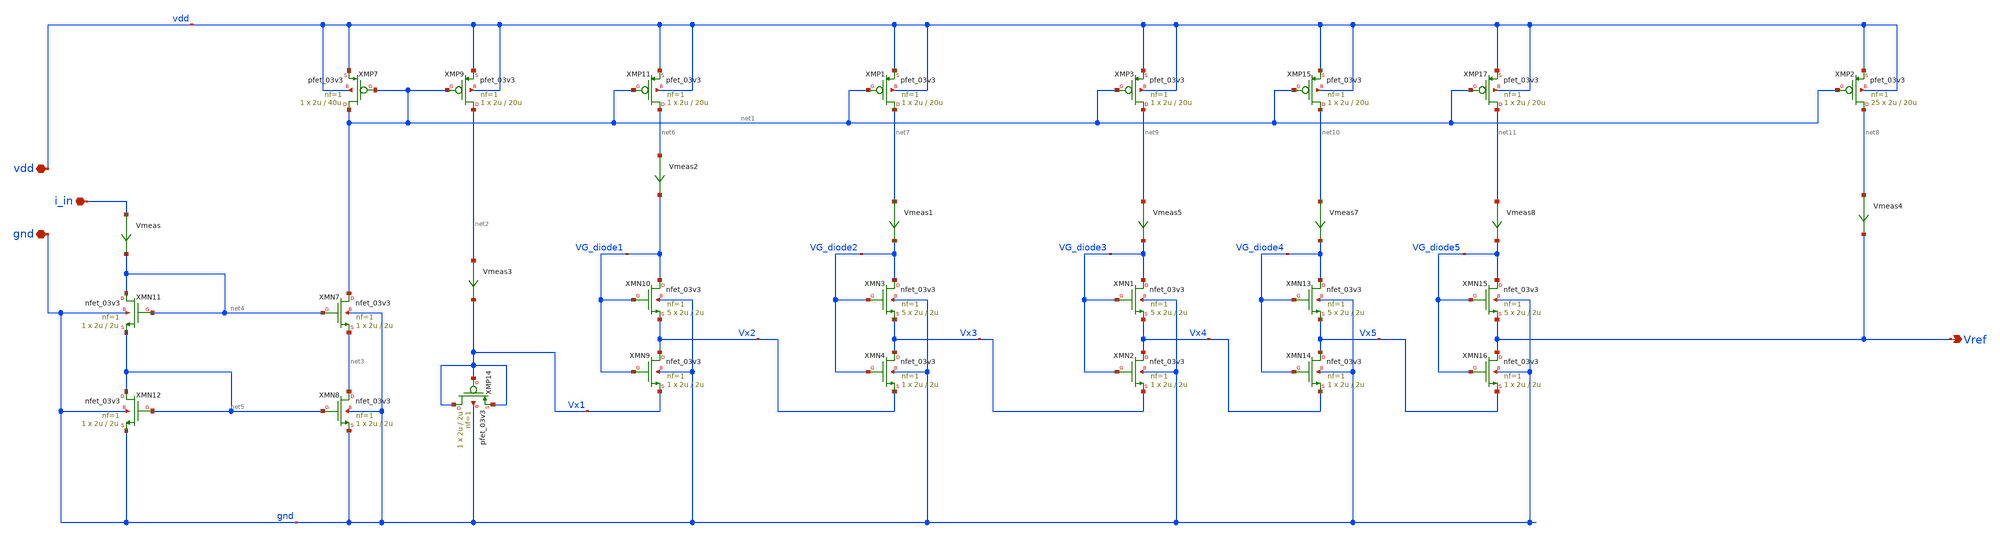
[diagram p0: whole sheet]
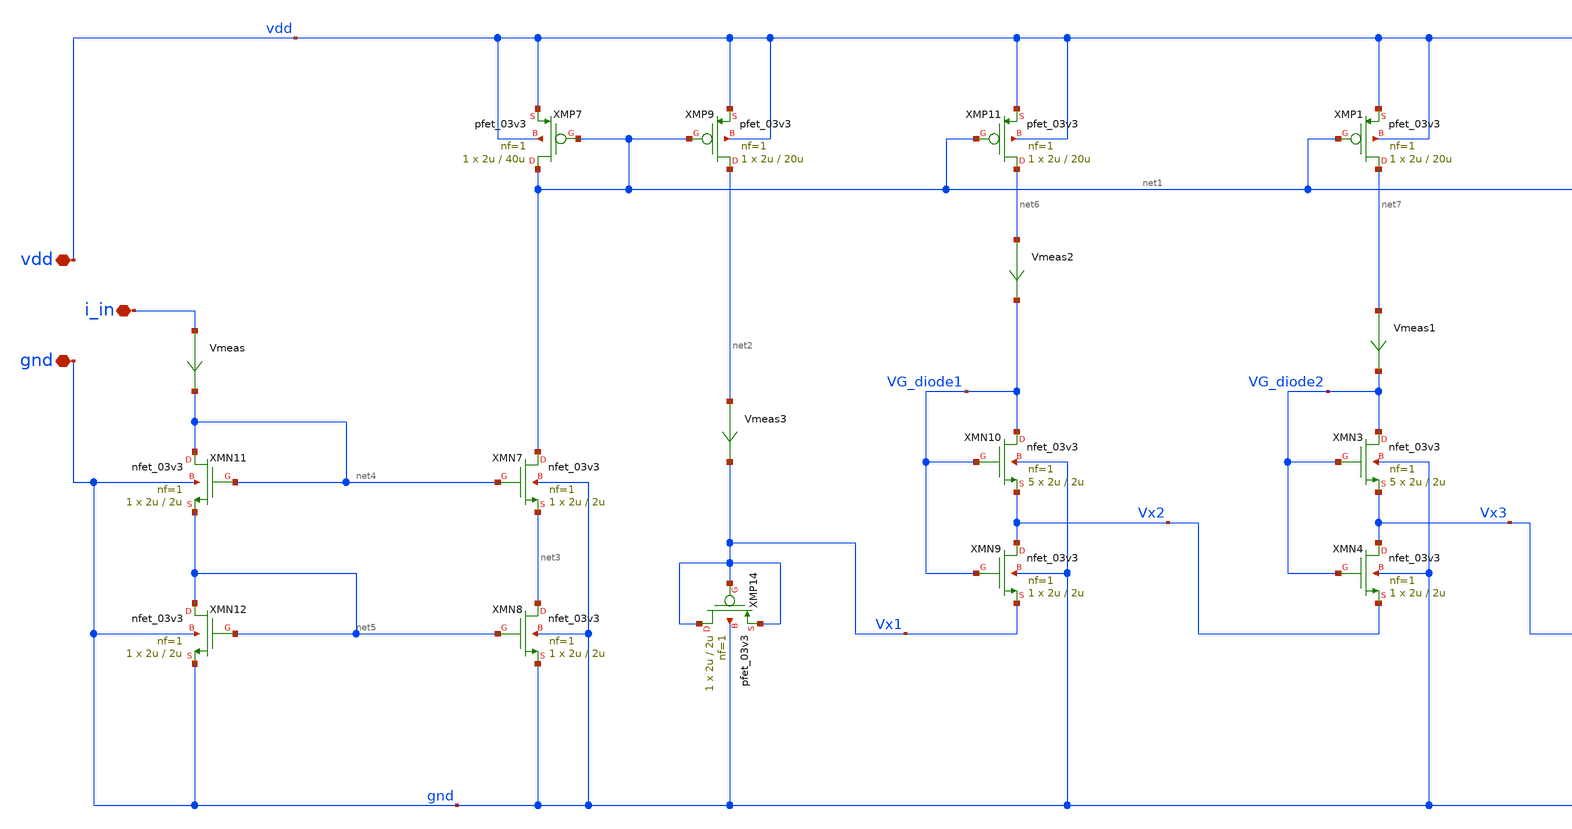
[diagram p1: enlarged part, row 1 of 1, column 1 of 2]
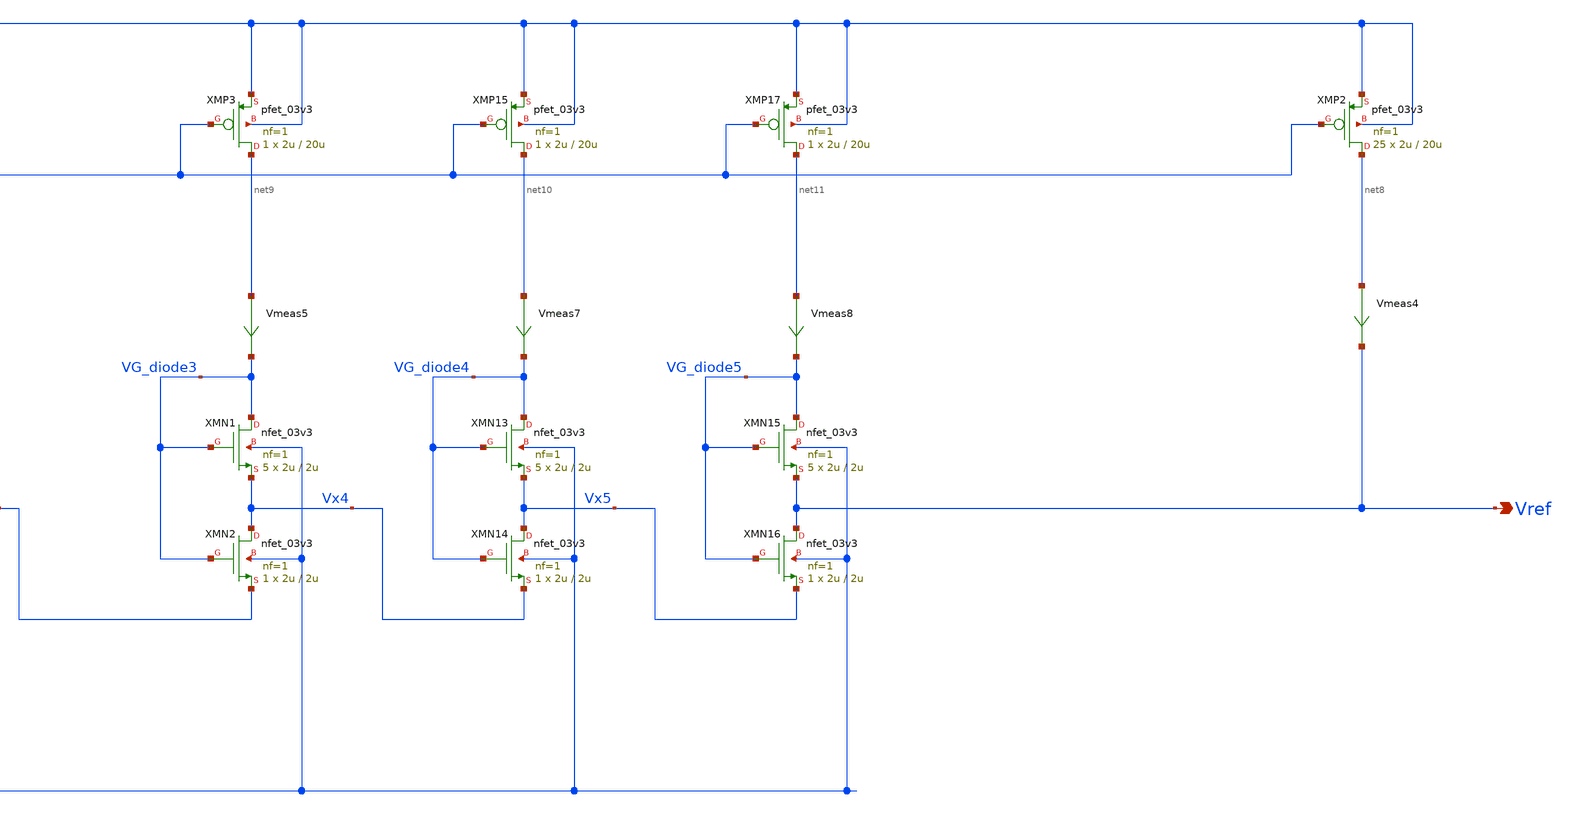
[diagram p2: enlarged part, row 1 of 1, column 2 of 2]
** sch_path: Voltage_Reference/symbols_vr/Voltage_Reference.sch
**.subckt Voltage_Reference i_in vdd gnd Vref
*.iopin i_in
*.iopin vdd
*.iopin gnd
*.opin Vref
XMP7 net1 net1 vdd vdd pfet_03v3 L=40u W=2u nf=1 ad='int((nf+1)/2) * W/nf * 0.18u' as='int((nf+2)/2) * W/nf * 0.18u'
+ pd='2*int((nf+1)/2) * (W/nf + 0.18u)' ps='2*int((nf+2)/2) * (W/nf + 0.18u)' nrd='0.18u / W' nrs='0.18u / W'
+ sa=0 sb=0 sd=0 m=1
XMP9 net2 net1 vdd vdd pfet_03v3 L=20u W=2u nf=1 ad='int((nf+1)/2) * W/nf * 0.18u' as='int((nf+2)/2) * W/nf * 0.18u'
+ pd='2*int((nf+1)/2) * (W/nf + 0.18u)' ps='2*int((nf+2)/2) * (W/nf + 0.18u)' nrd='0.18u / W' nrs='0.18u / W'
+ sa=0 sb=0 sd=0 m=1
XMN7 net1 net4 net3 gnd nfet_03v3 L=2u W=2u nf=1 ad='int((nf+1)/2) * W/nf * 0.18u' as='int((nf+2)/2) * W/nf * 0.18u'
+ pd='2*int((nf+1)/2) * (W/nf + 0.18u)' ps='2*int((nf+2)/2) * (W/nf + 0.18u)' nrd='0.18u / W' nrs='0.18u / W'
+ sa=0 sb=0 sd=0 m=1
XMN8 net3 net5 gnd gnd nfet_03v3 L=2u W=2u nf=1 ad='int((nf+1)/2) * W/nf * 0.18u' as='int((nf+2)/2) * W/nf * 0.18u'
+ pd='2*int((nf+1)/2) * (W/nf + 0.18u)' ps='2*int((nf+2)/2) * (W/nf + 0.18u)' nrd='0.18u / W' nrs='0.18u / W'
+ sa=0 sb=0 sd=0 m=1
XMP14 Vx1 Vx1 Vx1 gnd pfet_03v3 L=2u W=2u nf=1 ad='int((nf+1)/2) * W/nf * 0.18u' as='int((nf+2)/2) * W/nf * 0.18u'
+ pd='2*int((nf+1)/2) * (W/nf + 0.18u)' ps='2*int((nf+2)/2) * (W/nf + 0.18u)' nrd='0.18u / W' nrs='0.18u / W'
+ sa=0 sb=0 sd=0 m=1
XMP11 net6 net1 vdd vdd pfet_03v3 L=20u W=2u nf=1 ad='int((nf+1)/2) * W/nf * 0.18u' as='int((nf+2)/2) * W/nf * 0.18u'
+ pd='2*int((nf+1)/2) * (W/nf + 0.18u)' ps='2*int((nf+2)/2) * (W/nf + 0.18u)' nrd='0.18u / W' nrs='0.18u / W'
+ sa=0 sb=0 sd=0 m=1
XMN10 VG_diode1 VG_diode1 Vx2 gnd nfet_03v3 L=2u W=2u nf=1 ad='int((nf+1)/2) * W/nf * 0.18u' as='int((nf+2)/2) * W/nf * 0.18u'
+ pd='2*int((nf+1)/2) * (W/nf + 0.18u)' ps='2*int((nf+2)/2) * (W/nf + 0.18u)' nrd='0.18u / W' nrs='0.18u / W'
+ sa=0 sb=0 sd=0 m=5
XMN9 Vx2 VG_diode1 Vx1 gnd nfet_03v3 L=2u W=2u nf=1 ad='int((nf+1)/2) * W/nf * 0.18u' as='int((nf+2)/2) * W/nf * 0.18u'
+ pd='2*int((nf+1)/2) * (W/nf + 0.18u)' ps='2*int((nf+2)/2) * (W/nf + 0.18u)' nrd='0.18u / W' nrs='0.18u / W'
+ sa=0 sb=0 sd=0 m=1
XMN11 net4 net4 net5 gnd nfet_03v3 L=2u W=2u nf=1 ad='int((nf+1)/2) * W/nf * 0.18u' as='int((nf+2)/2) * W/nf * 0.18u'
+ pd='2*int((nf+1)/2) * (W/nf + 0.18u)' ps='2*int((nf+2)/2) * (W/nf + 0.18u)' nrd='0.18u / W' nrs='0.18u / W'
+ sa=0 sb=0 sd=0 m=1
XMN12 net5 net5 gnd gnd nfet_03v3 L=2u W=2u nf=1 ad='int((nf+1)/2) * W/nf * 0.18u' as='int((nf+2)/2) * W/nf * 0.18u'
+ pd='2*int((nf+1)/2) * (W/nf + 0.18u)' ps='2*int((nf+2)/2) * (W/nf + 0.18u)' nrd='0.18u / W' nrs='0.18u / W'
+ sa=0 sb=0 sd=0 m=1
Vmeas i_in net4 0
.save i(vmeas)
Vmeas3 net2 Vx1 0
.save i(vmeas3)
XMN3 VG_diode2 VG_diode2 Vx3 gnd nfet_03v3 L=2u W=2u nf=1 ad='int((nf+1)/2) * W/nf * 0.18u' as='int((nf+2)/2) * W/nf * 0.18u'
+ pd='2*int((nf+1)/2) * (W/nf + 0.18u)' ps='2*int((nf+2)/2) * (W/nf + 0.18u)' nrd='0.18u / W' nrs='0.18u / W'
+ sa=0 sb=0 sd=0 m=5
XMN4 Vx3 VG_diode2 Vx2 gnd nfet_03v3 L=2u W=2u nf=1 ad='int((nf+1)/2) * W/nf * 0.18u' as='int((nf+2)/2) * W/nf * 0.18u'
+ pd='2*int((nf+1)/2) * (W/nf + 0.18u)' ps='2*int((nf+2)/2) * (W/nf + 0.18u)' nrd='0.18u / W' nrs='0.18u / W'
+ sa=0 sb=0 sd=0 m=1
Vmeas1 net7 VG_diode2 0
.save i(vmeas1)
Vmeas2 net6 VG_diode1 0
.save i(vmeas2)
XMP1 net7 net1 vdd vdd pfet_03v3 L=20u W=2u nf=1 ad='int((nf+1)/2) * W/nf * 0.18u' as='int((nf+2)/2) * W/nf * 0.18u'
+ pd='2*int((nf+1)/2) * (W/nf + 0.18u)' ps='2*int((nf+2)/2) * (W/nf + 0.18u)' nrd='0.18u / W' nrs='0.18u / W'
+ sa=0 sb=0 sd=0 m=1
XMP2 net8 net1 vdd vdd pfet_03v3 L=20u W=2u nf=1 ad='int((nf+1)/2) * W/nf * 0.18u' as='int((nf+2)/2) * W/nf * 0.18u'
+ pd='2*int((nf+1)/2) * (W/nf + 0.18u)' ps='2*int((nf+2)/2) * (W/nf + 0.18u)' nrd='0.18u / W' nrs='0.18u / W'
+ sa=0 sb=0 sd=0 m=25
Vmeas4 net8 Vref 0
.save i(vmeas4)
XMN1 VG_diode3 VG_diode3 Vx4 gnd nfet_03v3 L=2u W=2u nf=1 ad='int((nf+1)/2) * W/nf * 0.18u' as='int((nf+2)/2) * W/nf * 0.18u'
+ pd='2*int((nf+1)/2) * (W/nf + 0.18u)' ps='2*int((nf+2)/2) * (W/nf + 0.18u)' nrd='0.18u / W' nrs='0.18u / W'
+ sa=0 sb=0 sd=0 m=5
XMN2 Vx4 VG_diode3 Vx3 gnd nfet_03v3 L=2u W=2u nf=1 ad='int((nf+1)/2) * W/nf * 0.18u' as='int((nf+2)/2) * W/nf * 0.18u'
+ pd='2*int((nf+1)/2) * (W/nf + 0.18u)' ps='2*int((nf+2)/2) * (W/nf + 0.18u)' nrd='0.18u / W' nrs='0.18u / W'
+ sa=0 sb=0 sd=0 m=1
Vmeas5 net9 VG_diode3 0
.save i(vmeas5)
XMP3 net9 net1 vdd vdd pfet_03v3 L=20u W=2u nf=1 ad='int((nf+1)/2) * W/nf * 0.18u' as='int((nf+2)/2) * W/nf * 0.18u'
+ pd='2*int((nf+1)/2) * (W/nf + 0.18u)' ps='2*int((nf+2)/2) * (W/nf + 0.18u)' nrd='0.18u / W' nrs='0.18u / W'
+ sa=0 sb=0 sd=0 m=1
XMN13 VG_diode4 VG_diode4 Vx5 gnd nfet_03v3 L=2u W=2u nf=1 ad='int((nf+1)/2) * W/nf * 0.18u' as='int((nf+2)/2) * W/nf * 0.18u'
+ pd='2*int((nf+1)/2) * (W/nf + 0.18u)' ps='2*int((nf+2)/2) * (W/nf + 0.18u)' nrd='0.18u / W' nrs='0.18u / W'
+ sa=0 sb=0 sd=0 m=5
XMN14 Vx5 VG_diode4 Vx4 gnd nfet_03v3 L=2u W=2u nf=1 ad='int((nf+1)/2) * W/nf * 0.18u' as='int((nf+2)/2) * W/nf * 0.18u'
+ pd='2*int((nf+1)/2) * (W/nf + 0.18u)' ps='2*int((nf+2)/2) * (W/nf + 0.18u)' nrd='0.18u / W' nrs='0.18u / W'
+ sa=0 sb=0 sd=0 m=1
Vmeas7 net10 VG_diode4 0
.save i(vmeas7)
XMP15 net10 net1 vdd vdd pfet_03v3 L=20u W=2u nf=1 ad='int((nf+1)/2) * W/nf * 0.18u' as='int((nf+2)/2) * W/nf * 0.18u'
+ pd='2*int((nf+1)/2) * (W/nf + 0.18u)' ps='2*int((nf+2)/2) * (W/nf + 0.18u)' nrd='0.18u / W' nrs='0.18u / W'
+ sa=0 sb=0 sd=0 m=1
XMN15 VG_diode5 VG_diode5 Vref gnd nfet_03v3 L=2u W=2u nf=1 ad='int((nf+1)/2) * W/nf * 0.18u' as='int((nf+2)/2) * W/nf * 0.18u'
+ pd='2*int((nf+1)/2) * (W/nf + 0.18u)' ps='2*int((nf+2)/2) * (W/nf + 0.18u)' nrd='0.18u / W' nrs='0.18u / W'
+ sa=0 sb=0 sd=0 m=5
XMN16 Vref VG_diode5 Vx5 gnd nfet_03v3 L=2u W=2u nf=1 ad='int((nf+1)/2) * W/nf * 0.18u' as='int((nf+2)/2) * W/nf * 0.18u'
+ pd='2*int((nf+1)/2) * (W/nf + 0.18u)' ps='2*int((nf+2)/2) * (W/nf + 0.18u)' nrd='0.18u / W' nrs='0.18u / W'
+ sa=0 sb=0 sd=0 m=1
Vmeas8 net11 VG_diode5 0
.save i(vmeas8)
XMP17 net11 net1 vdd vdd pfet_03v3 L=20u W=2u nf=1 ad='int((nf+1)/2) * W/nf * 0.18u' as='int((nf+2)/2) * W/nf * 0.18u'
+ pd='2*int((nf+1)/2) * (W/nf + 0.18u)' ps='2*int((nf+2)/2) * (W/nf + 0.18u)' nrd='0.18u / W' nrs='0.18u / W'
+ sa=0 sb=0 sd=0 m=1
**.ends
.end
